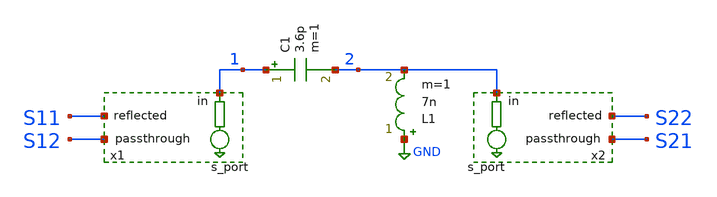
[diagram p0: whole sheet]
** sch_path: L-match_sparam.sch
**.subckt L-match_sparam
C1 1 2 3.6p m=1
L1 GND 2 7n m=1
x1 1 S12 S11 s_port Rbase=50 RS1=1e-6 RS2=1e12
x2 2 S21 S22 s_port Rbase=50 RS1=1e-6 RS2=1e12
**** begin user architecture code


.options method=gear
.options savecurrents
.save all

** Check the two ac lines below for being equal!
.control
set noaskquit
set filetype=ascii

** set input and output

alter R.x1.R1 = 1e-6
alter R.x1.R2 = 1e12
alter R.x2.R1 = 1e12
alter R.x2.R2 = 1e-6

*** measurement for s11 and s21
op
** first ac measurement (change this line only together with following ac line)
ac lin 200 0.1G 7G

**

** switch input and output

alter R.x1.R1 = 1e12
alter R.x1.R2 = 1e-6
alter R.x2.R1 = 1e-6
alter R.x2.R2 = 1e12

*** measurement for s12 and s22
op
** second ac measurement (change this line only together with ac line above)
ac lin 200 0.1G 7G

**

let s11=ac1.s11
let s21=ac1.s21
let s22=ac2.s22
let s12=ac2.s12
settype s-param s11 s21 s22 s12

let P11=180*ph(s11)/pi
let P21=180*ph(s21)/pi
let P22=180*ph(S22)/pi
let P12=180*ph(S12)/pi
settype phase P11 P21 P22 P12

let s11db = db(s11)
let s21db = db(s21)
let s22db = db(s22)
let s12db = db(s12)
settype decibel S11db S21db S22db S12db

let d = ((1-s11)*(1-s22)-s12*s21)
let z11 = ((1+s11)*(1-s22)+s12*s21) / d
let z12 = 2*s12 / d
let z21 = 2*s21 / d
let z22 = ((1-s11)*(1+s22)+s12*s21) / d
settype impedance z11 z21 z22 z11


*plot s11db s21db s22db s12db
plot xlog s11db s21db s22db s12db
*plot P11 P21 P22 P12
*plot smithgrid s11 s21 s22 s12

*plot z11 z22
plot xlog real(z11) imag(z11)
plot xlog real(z22) imag(z22)

.endc
.end

**** end user architecture code
**.ends

* expanding   symbol:  sparam/s_port.sym # of pins=3
** sym_path: sparam/s_port.sym
** sch_path: sparam/s_port.sch
.subckt s_port in passthrough reflected  Rbase=50 RS1=1e-6 RS2=1e12
*.iopin in
*.opin reflected
*.opin passthrough
Rout s2 8 Rbase m=1
Vdc 8 GND DC {Vbias_out} AC 0
E2 passthrough GND s2 GND 2
Vacdc 1 GND DC {Vbias_in} AC 1
Rin 1 s1 Rbase m=1
E1 3 GND s1 GND 2
Vac 3 4 DC 0 AC 1
Rloop reflected 4 1e-6 m=1
R3 reflected GND 1 m=1
.param Vbias_in = 0
R1 in s1 {RS1} m=1
R2 in s2 {RS2} m=1
.param Vbias_out = 0
.ends

.GLOBAL GND
.end
